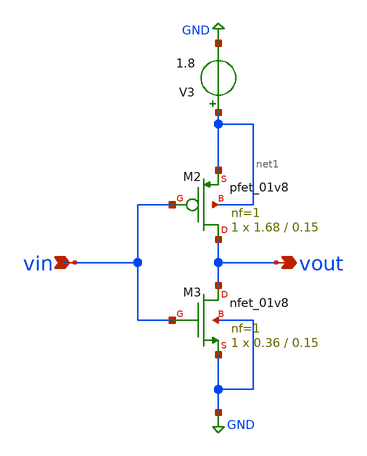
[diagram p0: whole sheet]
** sch_path: inverter.sch
**.subckt inverter vin vout
*.ipin vin
*.opin vout
XM2 vout vin net1 net1 sky130_fd_pr__pfet_01v8 L=0.15 W=1.68 nf=1 ad='int((nf+1)/2) * W/nf * 0.29' as='int((nf+2)/2) * W/nf * 0.29'
+ pd='2*int((nf+1)/2) * (W/nf + 0.29)' ps='2*int((nf+2)/2) * (W/nf + 0.29)' nrd='0.29 / W' nrs='0.29 / W'
+ sa=0 sb=0 sd=0 mult=1 m=1
XM3 vout vin GND GND sky130_fd_pr__nfet_01v8 L=0.15 W=0.36 nf=1 ad='int((nf+1)/2) * W/nf * 0.29' as='int((nf+2)/2) * W/nf * 0.29'
+ pd='2*int((nf+1)/2) * (W/nf + 0.29)' ps='2*int((nf+2)/2) * (W/nf + 0.29)' nrd='0.29 / W' nrs='0.29 / W'
+ sa=0 sb=0 sd=0 mult=1 m=1
V3 net1 GND 1.8
**.ends
.GLOBAL GND
.end
